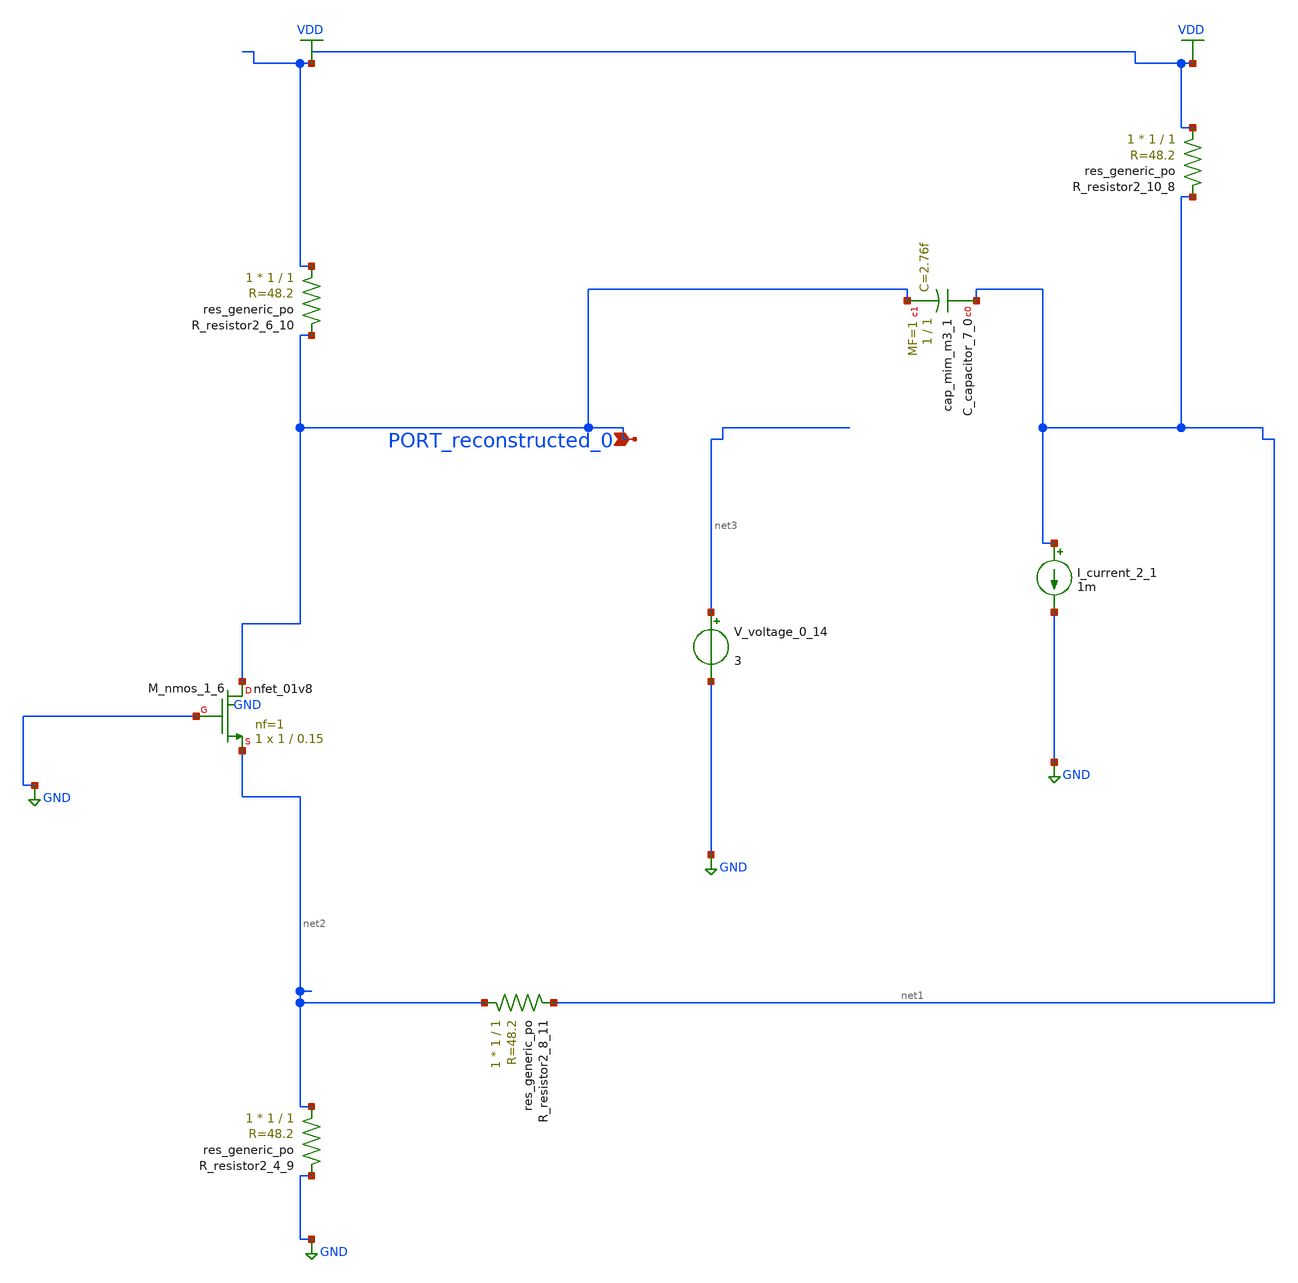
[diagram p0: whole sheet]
** sch_path: schematics/AMSNet/600.sch
**.subckt 600 PORT_reconstructed_0
*.ipin PORT_reconstructed_0
XC_capacitor_7_0 net1 PORT_reconstructed_0 sky130_fd_pr__cap_mim_m3_1 W=1 L=1 MF=1 m=1
I_current_2_1 net1 GND 1m
XM_nmos_1_6 PORT_reconstructed_0 GND net2 GND sky130_fd_pr__nfet_01v8 L=0.15 W=1 nf=1 ad='int((1 + 1)/2) * 1 / 1 * 0.29'
+ as='int((1 + 2)/2) * 1 / 1 * 0.29' pd='2*int((1 + 1)/2) * (1 / 1 + 0.29)' ps='2*int((1 + 2)/2) * (1 / 1 + 0.29)'
+ nrd='0.29 / 1 ' nrs='0.29 / 1 ' sa=0 sb=0 sd=0 mult=1 m=1
XR_resistor2_10_8 VDD net1 sky130_fd_pr__res_generic_po W=1 L=1 m=1
XR_resistor2_4_9 net2 GND sky130_fd_pr__res_generic_po W=1 L=1 m=1
XR_resistor2_6_10 VDD PORT_reconstructed_0 sky130_fd_pr__res_generic_po W=1 L=1 m=1
XR_resistor2_8_11 net2 net1 sky130_fd_pr__res_generic_po W=1 L=1 m=1
V_voltage_0_14 net3 GND 3
**.ends
.GLOBAL GND
.GLOBAL VDD
.end
